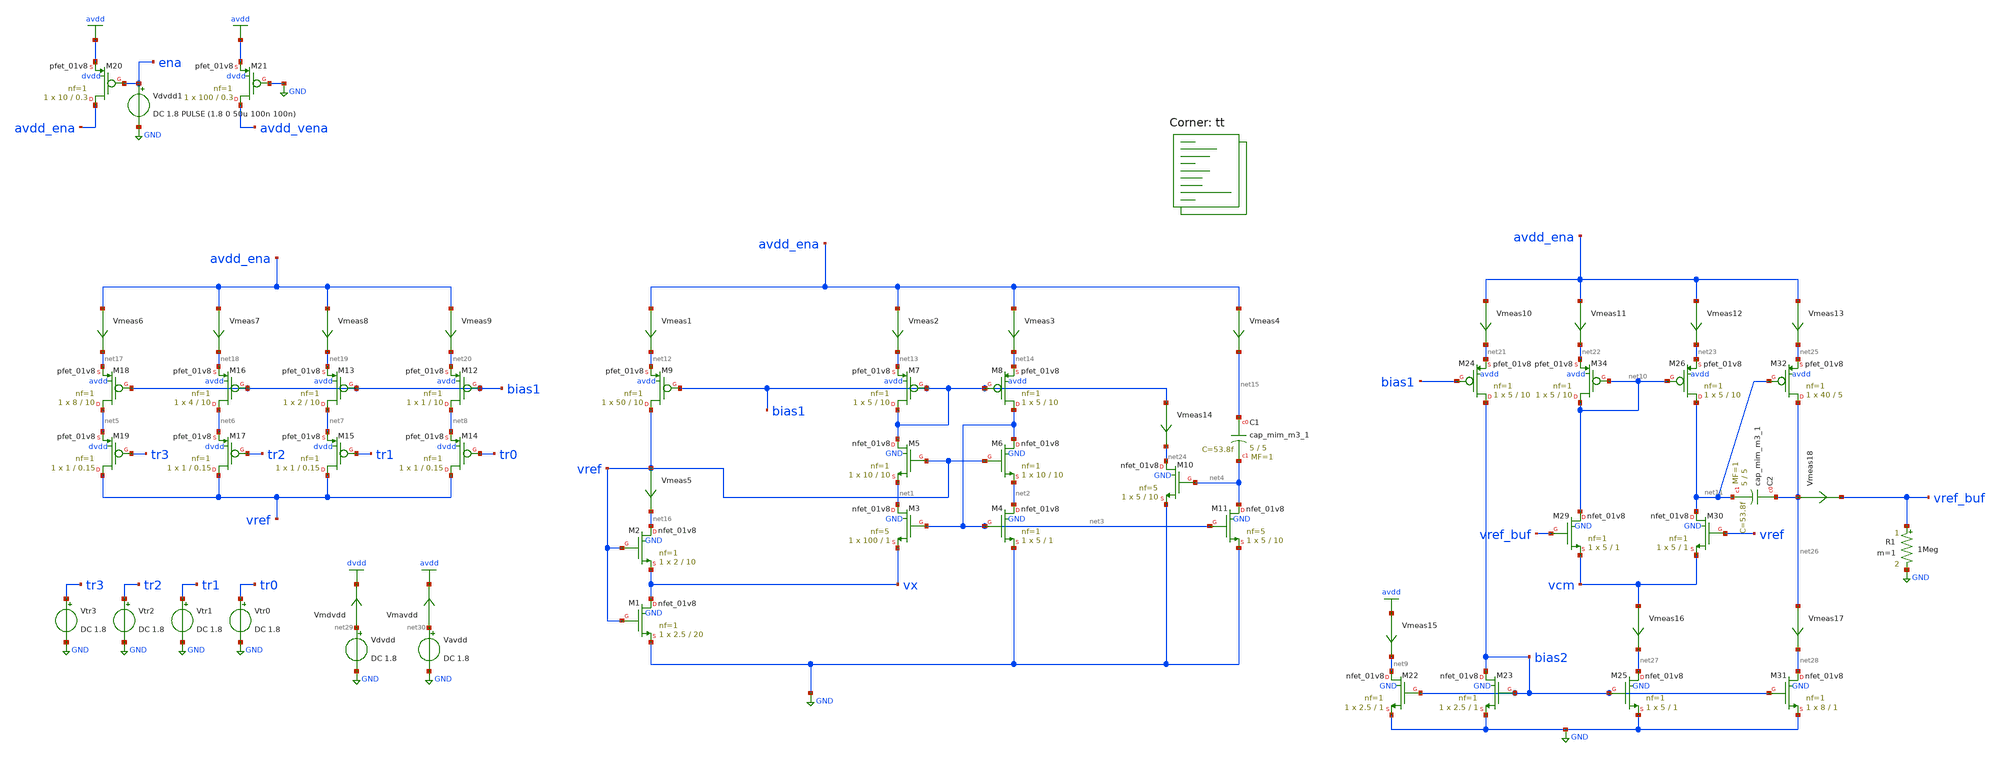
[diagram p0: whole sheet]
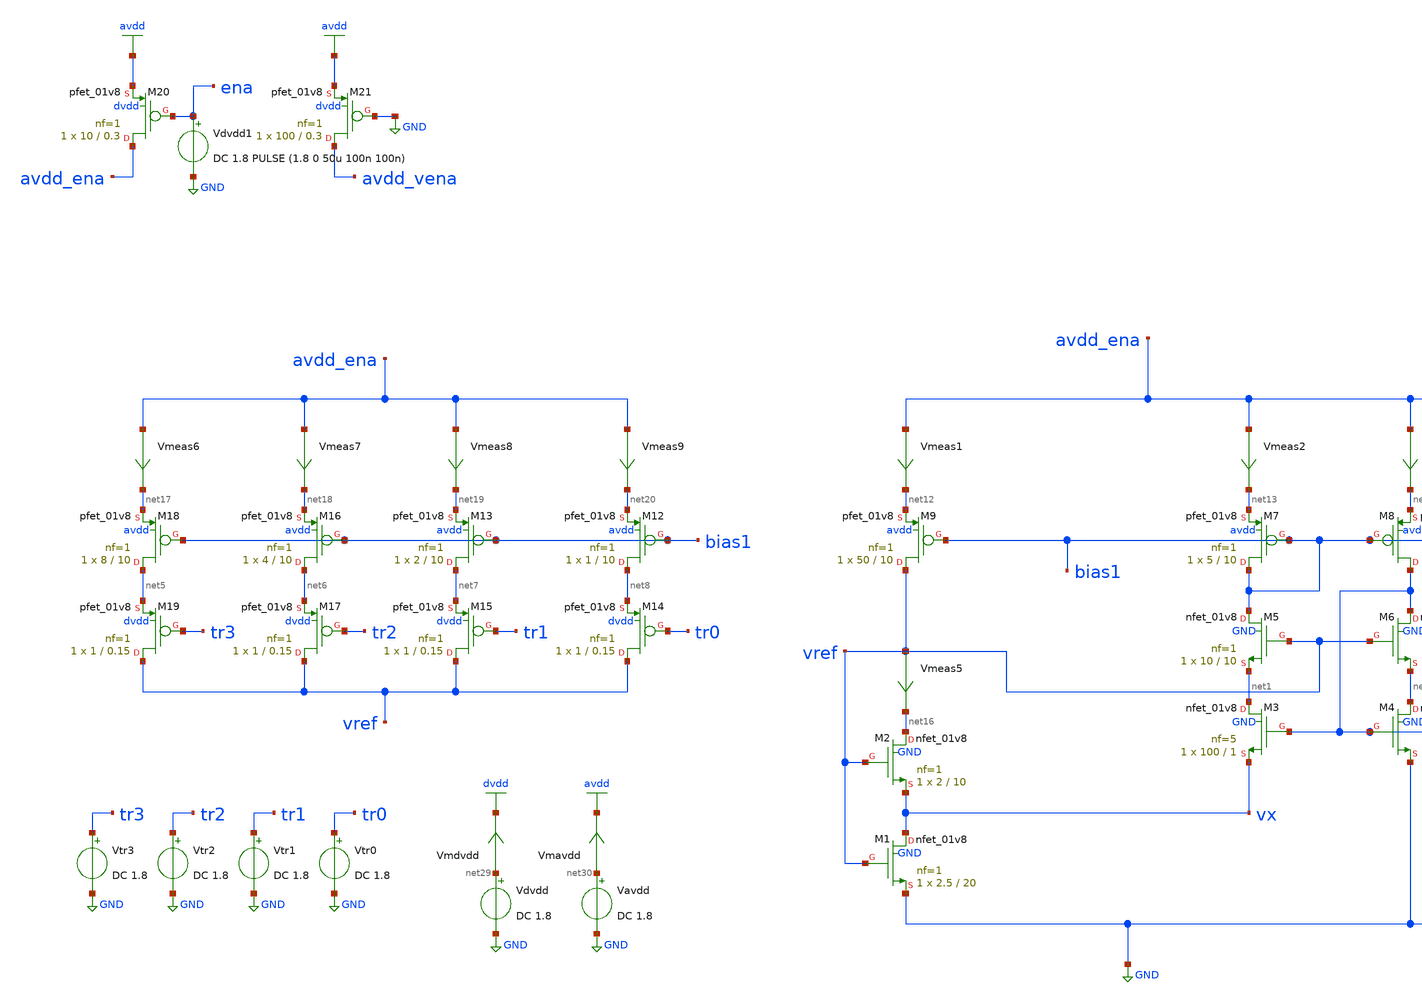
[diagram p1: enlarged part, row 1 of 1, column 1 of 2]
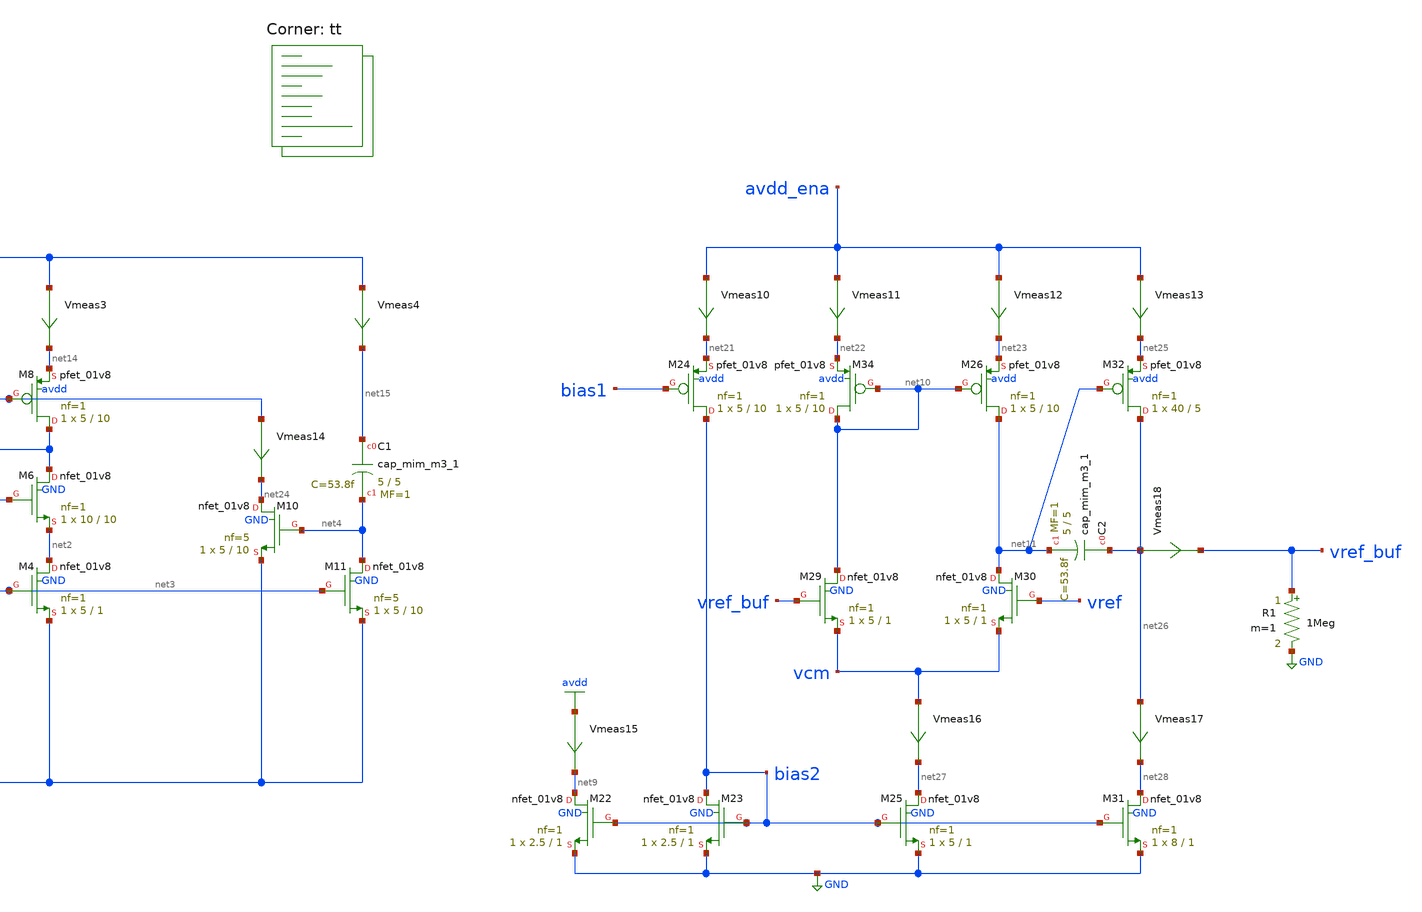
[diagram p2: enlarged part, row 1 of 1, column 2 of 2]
** sch_path: xschem/cmos_vref_design.sch
**.subckt cmos_vref_design
XM2 net16 vref vx GND sky130_fd_pr__nfet_01v8 L=10 W=2 nf=1 ad='int((nf+1)/2) * W/nf * 0.29' as='int((nf+2)/2) * W/nf * 0.29'
+ pd='2*int((nf+1)/2) * (W/nf + 0.29)' ps='2*int((nf+2)/2) * (W/nf + 0.29)' nrd='0.29 / W' nrs='0.29 / W'
+ sa=0 sb=0 sd=0 mult=1 m=1
XM1 vx vref GND GND sky130_fd_pr__nfet_01v8 L=20 W=2.5 nf=1 ad='int((nf+1)/2) * W/nf * 0.29' as='int((nf+2)/2) * W/nf * 0.29'
+ pd='2*int((nf+1)/2) * (W/nf + 0.29)' ps='2*int((nf+2)/2) * (W/nf + 0.29)' nrd='0.29 / W' nrs='0.29 / W'
+ sa=0 sb=0 sd=0 mult=1 m=1
XM3 net1 net3 vx GND sky130_fd_pr__nfet_01v8 L=1 W=100 nf=5 ad='int((nf+1)/2) * W/nf * 0.29' as='int((nf+2)/2) * W/nf * 0.29'
+ pd='2*int((nf+1)/2) * (W/nf + 0.29)' ps='2*int((nf+2)/2) * (W/nf + 0.29)' nrd='0.29 / W' nrs='0.29 / W'
+ sa=0 sb=0 sd=0 mult=1 m=1
XM4 net2 net3 GND GND sky130_fd_pr__nfet_01v8 L=1 W=5 nf=1 ad='int((nf+1)/2) * W/nf * 0.29' as='int((nf+2)/2) * W/nf * 0.29'
+ pd='2*int((nf+1)/2) * (W/nf + 0.29)' ps='2*int((nf+2)/2) * (W/nf + 0.29)' nrd='0.29 / W' nrs='0.29 / W'
+ sa=0 sb=0 sd=0 mult=1 m=1
XM5 bias1 vref net1 GND sky130_fd_pr__nfet_01v8 L=10 W=10 nf=1 ad='int((nf+1)/2) * W/nf * 0.29' as='int((nf+2)/2) * W/nf * 0.29'
+ pd='2*int((nf+1)/2) * (W/nf + 0.29)' ps='2*int((nf+2)/2) * (W/nf + 0.29)' nrd='0.29 / W' nrs='0.29 / W'
+ sa=0 sb=0 sd=0 mult=1 m=1
XM6 net3 vref net2 GND sky130_fd_pr__nfet_01v8 L=10 W=10 nf=1 ad='int((nf+1)/2) * W/nf * 0.29' as='int((nf+2)/2) * W/nf * 0.29'
+ pd='2*int((nf+1)/2) * (W/nf + 0.29)' ps='2*int((nf+2)/2) * (W/nf + 0.29)' nrd='0.29 / W' nrs='0.29 / W'
+ sa=0 sb=0 sd=0 mult=1 m=1
XM7 bias1 bias1 net13 avdd sky130_fd_pr__pfet_01v8 L=10 W=5 nf=1 ad='int((nf+1)/2) * W/nf * 0.29' as='int((nf+2)/2) * W/nf * 0.29'
+ pd='2*int((nf+1)/2) * (W/nf + 0.29)' ps='2*int((nf+2)/2) * (W/nf + 0.29)' nrd='0.29 / W' nrs='0.29 / W'
+ sa=0 sb=0 sd=0 mult=1 m=1
XM8 net3 bias1 net14 avdd sky130_fd_pr__pfet_01v8 L=10 W=5 nf=1 ad='int((nf+1)/2) * W/nf * 0.29' as='int((nf+2)/2) * W/nf * 0.29'
+ pd='2*int((nf+1)/2) * (W/nf + 0.29)' ps='2*int((nf+2)/2) * (W/nf + 0.29)' nrd='0.29 / W' nrs='0.29 / W'
+ sa=0 sb=0 sd=0 mult=1 m=1
XM9 vref bias1 net12 avdd sky130_fd_pr__pfet_01v8 L=10 W=50 nf=1 ad='int((nf+1)/2) * W/nf * 0.29' as='int((nf+2)/2) * W/nf * 0.29'
+ pd='2*int((nf+1)/2) * (W/nf + 0.29)' ps='2*int((nf+2)/2) * (W/nf + 0.29)' nrd='0.29 / W' nrs='0.29 / W'
+ sa=0 sb=0 sd=0 mult=1 m=1
XM12 net8 bias1 net20 avdd sky130_fd_pr__pfet_01v8 L=10 W=1 nf=1 ad='int((nf+1)/2) * W/nf * 0.29' as='int((nf+2)/2) * W/nf * 0.29'
+ pd='2*int((nf+1)/2) * (W/nf + 0.29)' ps='2*int((nf+2)/2) * (W/nf + 0.29)' nrd='0.29 / W' nrs='0.29 / W'
+ sa=0 sb=0 sd=0 mult=1 m=1
XM13 net7 bias1 net19 avdd sky130_fd_pr__pfet_01v8 L=10 W=2 nf=1 ad='int((nf+1)/2) * W/nf * 0.29' as='int((nf+2)/2) * W/nf * 0.29'
+ pd='2*int((nf+1)/2) * (W/nf + 0.29)' ps='2*int((nf+2)/2) * (W/nf + 0.29)' nrd='0.29 / W' nrs='0.29 / W'
+ sa=0 sb=0 sd=0 mult=1 m=1
XM14 vref tr0 net8 dvdd sky130_fd_pr__pfet_01v8 L=0.15 W=1 nf=1 ad='int((nf+1)/2) * W/nf * 0.29' as='int((nf+2)/2) * W/nf * 0.29'
+ pd='2*int((nf+1)/2) * (W/nf + 0.29)' ps='2*int((nf+2)/2) * (W/nf + 0.29)' nrd='0.29 / W' nrs='0.29 / W'
+ sa=0 sb=0 sd=0 mult=1 m=1
XM15 vref tr1 net7 dvdd sky130_fd_pr__pfet_01v8 L=0.15 W=1 nf=1 ad='int((nf+1)/2) * W/nf * 0.29' as='int((nf+2)/2) * W/nf * 0.29'
+ pd='2*int((nf+1)/2) * (W/nf + 0.29)' ps='2*int((nf+2)/2) * (W/nf + 0.29)' nrd='0.29 / W' nrs='0.29 / W'
+ sa=0 sb=0 sd=0 mult=1 m=1
XM16 net6 bias1 net18 avdd sky130_fd_pr__pfet_01v8 L=10 W=4 nf=1 ad='int((nf+1)/2) * W/nf * 0.29' as='int((nf+2)/2) * W/nf * 0.29'
+ pd='2*int((nf+1)/2) * (W/nf + 0.29)' ps='2*int((nf+2)/2) * (W/nf + 0.29)' nrd='0.29 / W' nrs='0.29 / W'
+ sa=0 sb=0 sd=0 mult=1 m=1
XM17 vref tr2 net6 dvdd sky130_fd_pr__pfet_01v8 L=0.15 W=1 nf=1 ad='int((nf+1)/2) * W/nf * 0.29' as='int((nf+2)/2) * W/nf * 0.29'
+ pd='2*int((nf+1)/2) * (W/nf + 0.29)' ps='2*int((nf+2)/2) * (W/nf + 0.29)' nrd='0.29 / W' nrs='0.29 / W'
+ sa=0 sb=0 sd=0 mult=1 m=1
XM18 net5 bias1 net17 avdd sky130_fd_pr__pfet_01v8 L=10 W=8 nf=1 ad='int((nf+1)/2) * W/nf * 0.29' as='int((nf+2)/2) * W/nf * 0.29'
+ pd='2*int((nf+1)/2) * (W/nf + 0.29)' ps='2*int((nf+2)/2) * (W/nf + 0.29)' nrd='0.29 / W' nrs='0.29 / W'
+ sa=0 sb=0 sd=0 mult=1 m=1
XM19 vref tr3 net5 dvdd sky130_fd_pr__pfet_01v8 L=0.15 W=1 nf=1 ad='int((nf+1)/2) * W/nf * 0.29' as='int((nf+2)/2) * W/nf * 0.29'
+ pd='2*int((nf+1)/2) * (W/nf + 0.29)' ps='2*int((nf+2)/2) * (W/nf + 0.29)' nrd='0.29 / W' nrs='0.29 / W'
+ sa=0 sb=0 sd=0 mult=1 m=1
XM20 avdd_ena ena avdd dvdd sky130_fd_pr__pfet_01v8 L=0.3 W=10 nf=1 ad='int((nf+1)/2) * W/nf * 0.29'
+ as='int((nf+2)/2) * W/nf * 0.29' pd='2*int((nf+1)/2) * (W/nf + 0.29)' ps='2*int((nf+2)/2) * (W/nf + 0.29)'
+ nrd='0.29 / W' nrs='0.29 / W' sa=0 sb=0 sd=0 mult=1 m=1
XM21 avdd_vena GND avdd dvdd sky130_fd_pr__pfet_01v8 L=0.3 W=100 nf=1 ad='int((nf+1)/2) * W/nf * 0.29'
+ as='int((nf+2)/2) * W/nf * 0.29' pd='2*int((nf+1)/2) * (W/nf + 0.29)' ps='2*int((nf+2)/2) * (W/nf + 0.29)'
+ nrd='0.29 / W' nrs='0.29 / W' sa=0 sb=0 sd=0 mult=1 m=1
XM22 net9 bias2 GND GND sky130_fd_pr__nfet_01v8 L=1 W=2.5 nf=1 ad='int((nf+1)/2) * W/nf * 0.29' as='int((nf+2)/2) * W/nf * 0.29'
+ pd='2*int((nf+1)/2) * (W/nf + 0.29)' ps='2*int((nf+2)/2) * (W/nf + 0.29)' nrd='0.29 / W' nrs='0.29 / W'
+ sa=0 sb=0 sd=0 mult=1 m=1
XM23 bias2 bias2 GND GND sky130_fd_pr__nfet_01v8 L=1 W=2.5 nf=1 ad='int((nf+1)/2) * W/nf * 0.29' as='int((nf+2)/2) * W/nf * 0.29'
+ pd='2*int((nf+1)/2) * (W/nf + 0.29)' ps='2*int((nf+2)/2) * (W/nf + 0.29)' nrd='0.29 / W' nrs='0.29 / W'
+ sa=0 sb=0 sd=0 mult=1 m=1
XM24 bias2 bias1 net21 avdd sky130_fd_pr__pfet_01v8 L=10 W=5 nf=1 ad='int((nf+1)/2) * W/nf * 0.29' as='int((nf+2)/2) * W/nf * 0.29'
+ pd='2*int((nf+1)/2) * (W/nf + 0.29)' ps='2*int((nf+2)/2) * (W/nf + 0.29)' nrd='0.29 / W' nrs='0.29 / W'
+ sa=0 sb=0 sd=0 mult=1 m=1
XM25 net27 bias2 GND GND sky130_fd_pr__nfet_01v8 L=1 W=5 nf=1 ad='int((nf+1)/2) * W/nf * 0.29' as='int((nf+2)/2) * W/nf * 0.29'
+ pd='2*int((nf+1)/2) * (W/nf + 0.29)' ps='2*int((nf+2)/2) * (W/nf + 0.29)' nrd='0.29 / W' nrs='0.29 / W'
+ sa=0 sb=0 sd=0 mult=1 m=1
XM26 net11 net10 net23 avdd sky130_fd_pr__pfet_01v8 L=10 W=5 nf=1 ad='int((nf+1)/2) * W/nf * 0.29' as='int((nf+2)/2) * W/nf * 0.29'
+ pd='2*int((nf+1)/2) * (W/nf + 0.29)' ps='2*int((nf+2)/2) * (W/nf + 0.29)' nrd='0.29 / W' nrs='0.29 / W'
+ sa=0 sb=0 sd=0 mult=1 m=1
XM29 net10 vref_buf vcm GND sky130_fd_pr__nfet_01v8 L=1 W=5 nf=1 ad='int((nf+1)/2) * W/nf * 0.29' as='int((nf+2)/2) * W/nf * 0.29'
+ pd='2*int((nf+1)/2) * (W/nf + 0.29)' ps='2*int((nf+2)/2) * (W/nf + 0.29)' nrd='0.29 / W' nrs='0.29 / W'
+ sa=0 sb=0 sd=0 mult=1 m=1
XM30 net11 vref vcm GND sky130_fd_pr__nfet_01v8 L=1 W=5 nf=1 ad='int((nf+1)/2) * W/nf * 0.29' as='int((nf+2)/2) * W/nf * 0.29'
+ pd='2*int((nf+1)/2) * (W/nf + 0.29)' ps='2*int((nf+2)/2) * (W/nf + 0.29)' nrd='0.29 / W' nrs='0.29 / W'
+ sa=0 sb=0 sd=0 mult=1 m=1
XM34 net10 net10 net22 avdd sky130_fd_pr__pfet_01v8 L=10 W=5 nf=1 ad='int((nf+1)/2) * W/nf * 0.29' as='int((nf+2)/2) * W/nf * 0.29'
+ pd='2*int((nf+1)/2) * (W/nf + 0.29)' ps='2*int((nf+2)/2) * (W/nf + 0.29)' nrd='0.29 / W' nrs='0.29 / W'
+ sa=0 sb=0 sd=0 mult=1 m=1
XM10 net24 net4 GND GND sky130_fd_pr__nfet_01v8 L=10 W=5 nf=5 ad='int((nf+1)/2) * W/nf * 0.29' as='int((nf+2)/2) * W/nf * 0.29'
+ pd='2*int((nf+1)/2) * (W/nf + 0.29)' ps='2*int((nf+2)/2) * (W/nf + 0.29)' nrd='0.29 / W' nrs='0.29 / W'
+ sa=0 sb=0 sd=0 mult=1 m=1
XM11 net4 net3 GND GND sky130_fd_pr__nfet_01v8 L=10 W=5 nf=5 ad='int((nf+1)/2) * W/nf * 0.29' as='int((nf+2)/2) * W/nf * 0.29'
+ pd='2*int((nf+1)/2) * (W/nf + 0.29)' ps='2*int((nf+2)/2) * (W/nf + 0.29)' nrd='0.29 / W' nrs='0.29 / W'
+ sa=0 sb=0 sd=0 mult=1 m=1
XC1 net15 net4 sky130_fd_pr__cap_mim_m3_1 W=5 L=5 MF=1 m=1
Vmeas1 avdd_ena net12 0
.save i(vmeas1)
Vmeas2 avdd_ena net13 0
.save i(vmeas2)
Vmeas3 avdd_ena net14 0
.save i(vmeas3)
Vmeas4 avdd_ena net15 0
.save i(vmeas4)
Vmeas5 vref net16 0
.save i(vmeas5)
Vmeas6 avdd_ena net17 0
.save i(vmeas6)
Vmeas7 avdd_ena net18 0
.save i(vmeas7)
Vmeas8 avdd_ena net19 0
.save i(vmeas8)
Vmeas9 avdd_ena net20 0
.save i(vmeas9)
Vmeas10 avdd_ena net21 0
.save i(vmeas10)
Vmeas11 avdd_ena net22 0
.save i(vmeas11)
Vmeas12 avdd_ena net23 0
.save i(vmeas12)
Vmeas13 avdd_ena net25 0
.save i(vmeas13)
Vdvdd net29 GND DC 1.8
Vavdd net30 GND DC 1.8
Vtr0 tr0 GND DC 1.8
Vtr1 tr1 GND DC 1.8
Vtr2 tr2 GND DC 1.8
Vtr3 tr3 GND DC 1.8
Vmeas14 bias1 net24 0
.save i(vmeas14)
XM31 net28 bias2 GND GND sky130_fd_pr__nfet_01v8 L=1 W=8 nf=1 ad='int((nf+1)/2) * W/nf * 0.29' as='int((nf+2)/2) * W/nf * 0.29'
+ pd='2*int((nf+1)/2) * (W/nf + 0.29)' ps='2*int((nf+2)/2) * (W/nf + 0.29)' nrd='0.29 / W' nrs='0.29 / W'
+ sa=0 sb=0 sd=0 mult=1 m=1
XC2 net26 net11 sky130_fd_pr__cap_mim_m3_1 W=5 L=5 MF=1 m=1
XM32 net26 net11 net25 avdd sky130_fd_pr__pfet_01v8 L=5 W=40 nf=1 ad='int((nf+1)/2) * W/nf * 0.29' as='int((nf+2)/2) * W/nf * 0.29'
+ pd='2*int((nf+1)/2) * (W/nf + 0.29)' ps='2*int((nf+2)/2) * (W/nf + 0.29)' nrd='0.29 / W' nrs='0.29 / W'
+ sa=0 sb=0 sd=0 mult=1 m=1
Vmeas15 avdd net9 0
.save i(vmeas15)
Vmeas16 vcm net27 0
.save i(vmeas16)
Vmeas17 net26 net28 0
.save i(vmeas17)
Vmeas18 net26 vref_buf 0
.save i(vmeas18)
R1 vref_buf GND 1Meg m=1
Vmavdd net30 avdd 0
.save i(vmavdd)
Vmdvdd net29 dvdd 0
.save i(vmdvdd)
Vdvdd1 ena GND DC 1.8 PULSE (1.8 0 50u 100n 100n)
**** begin user architecture code
.lib $::SKYWATER_MODELS/sky130.lib.spice tt


.option warn=1
.control
save all
op
write vrefdesign_op.raw
dc TEMP -40 85 5
*dc Vavdd 0 1.92 50m
*tran 10n 100us 50us
*plot i(vmavdd), i(vmdvdd)
*plot vref_buf, vref
write vrefdesign_tempsweep.raw
.endc


**** end user architecture code
**.ends
.GLOBAL GND
.GLOBAL avdd
.GLOBAL dvdd
.end
